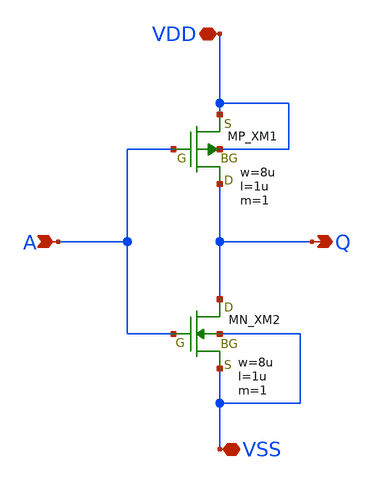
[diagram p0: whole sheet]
** sch_path: src/inverter_regymm.sch
**.subckt inverter_regymm A Q VDD VSS
*.ipin A
*.opin Q
*.iopin VDD
*.iopin VSS
XXM1 Q A VDD VDD PMOS w=8u l=1u as=0 ad=0 ps=0 pd=0 nrd=0 nrs=0 m=1
XXM2 Q A VSS VSS NMOS w=8u l=1u as=0 ad=0 ps=0 pd=0 nrd=0 nrs=0 m=1
**.ends
.end
